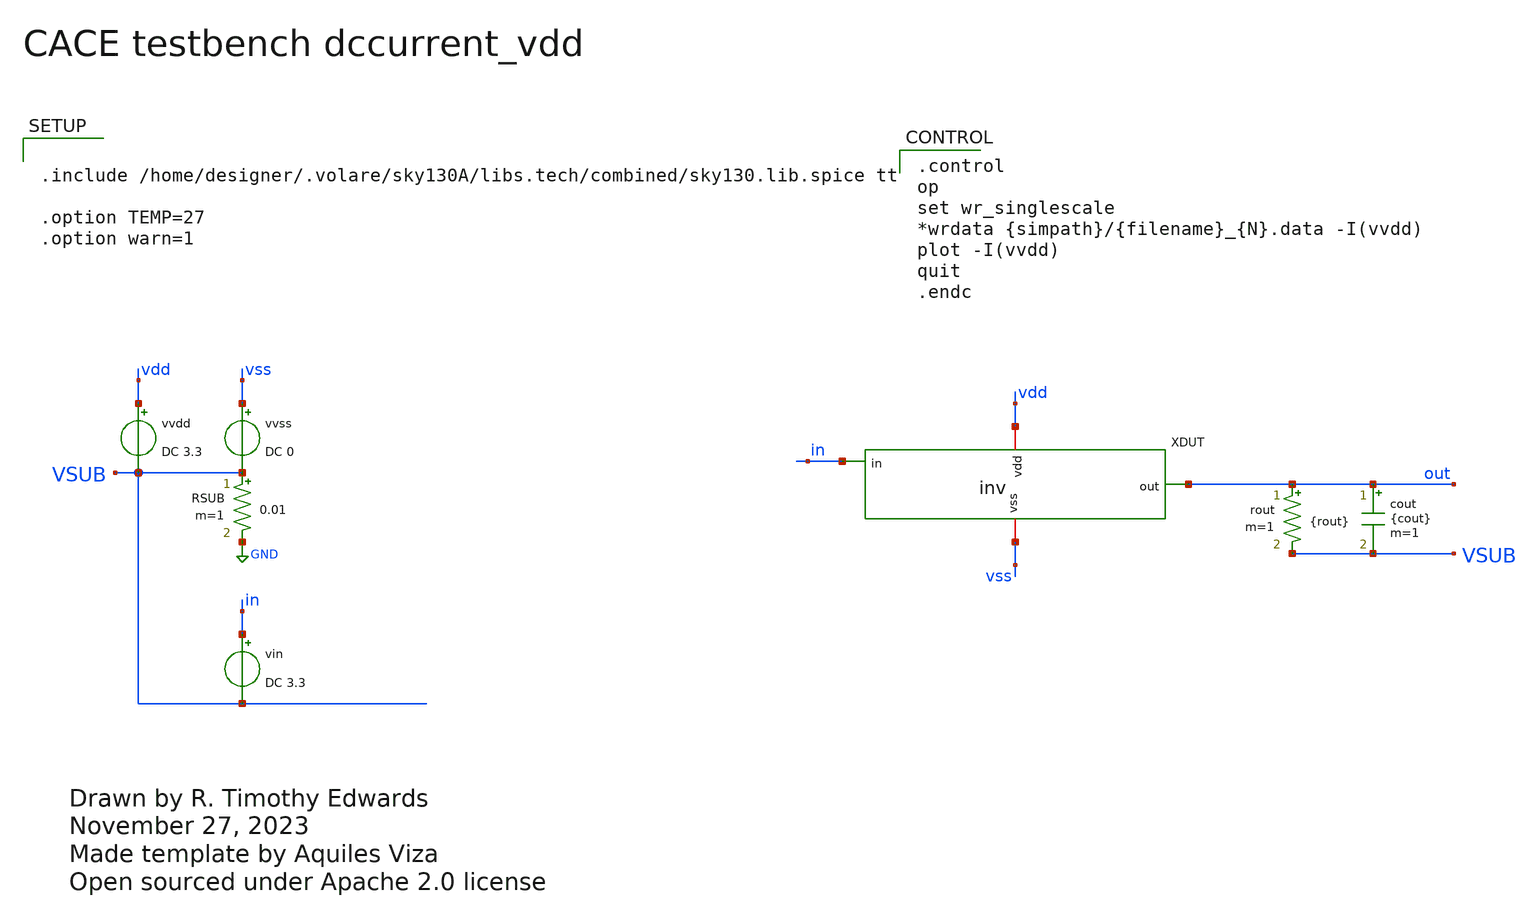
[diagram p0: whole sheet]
** sch_path: samples/cace-tests/inv/xschem/dccurrent_vdd.sch
* Open sourced under Apache 2.0 license


.include /home/designer/.volare/sky130A/libs.tech/combined/sky130.lib.spice tt

.option TEMP=27
.option warn=1


**.subckt dccurrent_vdd
vin in VSUB DC 3.3
vvss vss VSUB DC 0
rout out VSUB {rout} m=1
cout out VSUB {cout} m=1
vvdd vdd VSUB DC 3.3
RSUB VSUB GND 0.01 m=1
XDUT vdd in out vss inv
**** begin user architecture code

.control
op
set wr_singlescale
*wrdata {simpath}/{filename}_{N}.data -I(vvdd)
plot -I(vvdd)
quit
.endc


**** end user architecture code
**.ends

* expanding   symbol:  inv.sym # of pins=4
** sym_path: samples/cace-tests/inv/xschem/inv.sym
** sch_path: samples/cace-tests/inv/xschem/inv.sch
.subckt inv vdd in out vss
*.iopin vdd
*.iopin vss
*.ipin in
*.opin out
XM1 out in vdd VDD sky130_fd_pr__pfet_01v8 L=0.15 W=3 nf=1 ad='int((nf+1)/2) * W/nf * 0.29' as='int((nf+2)/2) * W/nf * 0.29'
+ pd='2*int((nf+1)/2) * (W/nf + 0.29)' ps='2*int((nf+2)/2) * (W/nf + 0.29)' nrd='0.29 / W' nrs='0.29 / W'
+ sa=0 sb=0 sd=0 mult=1 m=1
XM2 out in vss GND sky130_fd_pr__nfet_01v8 L=0.15 W=1 nf=1 ad='int((nf+1)/2) * W/nf * 0.29' as='int((nf+2)/2) * W/nf * 0.29'
+ pd='2*int((nf+1)/2) * (W/nf + 0.29)' ps='2*int((nf+2)/2) * (W/nf + 0.29)' nrd='0.29 / W' nrs='0.29 / W'
+ sa=0 sb=0 sd=0 mult=1 m=1
.ends

.GLOBAL GND
.end
